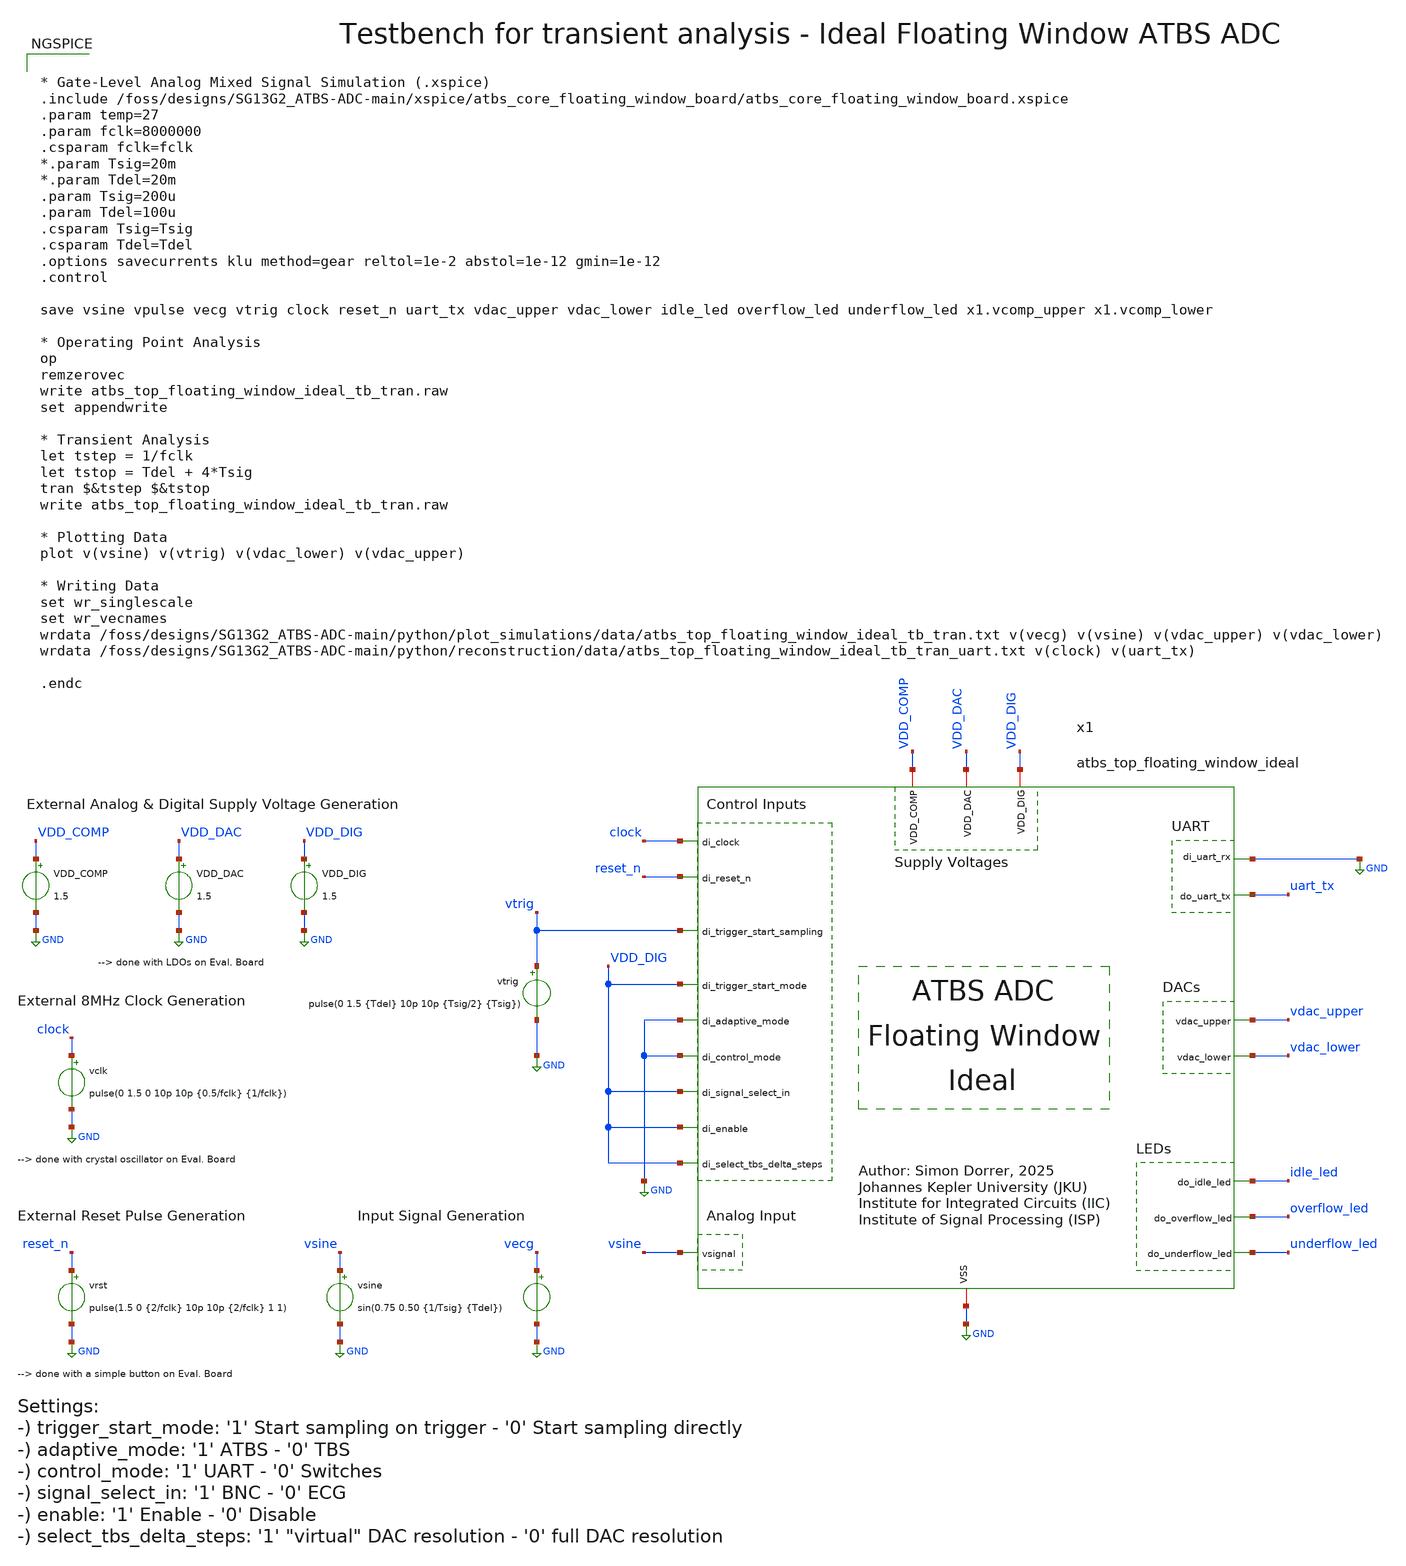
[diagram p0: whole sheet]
** sch_path: SG13G2_ATBS-ADC-main/xschem/top_level/testbenches/atbs_top_floating_window_ideal_tb_tran.sch
**.subckt atbs_top_floating_window_ideal_tb_tran
VDD_DAC VDD_DAC GND 1.5
VDD_COMP VDD_COMP GND 1.5
vsine vsine GND sin(0.75 0.50 {1/Tsig} {Tdel})
vclk clock GND pulse(0 1.5 0 10p 10p {0.5/fclk} {1/fclk})
vrst reset_n GND pulse(1.5 0 {2/fclk} 10p 10p {2/fclk} 1 1)
VDD_DIG VDD_DIG GND 1.5
x1 VDD_DIG VDD_COMP clock reset_n vtrig VDD_DAC VDD_DIG GND GND vsine VDD_DIG VDD_DIG VDD_DIG GND
+ uart_tx idle_led overflow_led underflow_led GND vdac_upper vdac_lower atbs_top_floating_window_ideal
vecg vecg GND dc 0 pwl(0.0 0.5958 3.910068426197458e-06 0.5985 7.820136852394917e-06 0.5982
+ 1.1730205278592374e-05 0.6038 1.5640273704789833e-05 0.61 1.9550342130987292e-05 0.6144 2.3460410557184748e-05 0.6189
+ 2.7370478983382207e-05 0.6204 3.1280547409579666e-05 0.6162 3.519061583577712e-05 0.6119 3.9100684261974585e-05 0.6106
+ 4.301075268817204e-05 0.6123 4.6920821114369496e-05 0.6199 5.083088954056696e-05 0.6267 5.4740957966764414e-05 0.6299
+ 5.865102639296188e-05 0.6252 6.256109481915933e-05 0.6185 6.647116324535679e-05 0.6128 7.038123167155424e-05 0.6143
+ 7.429130009775171e-05 0.6176 7.820136852394917e-05 0.6242 8.211143695014662e-05 0.6294 8.602150537634408e-05 0.6272
+ 8.993157380254154e-05 0.6273 9.384164222873899e-05 0.6275 9.775171065493646e-05 0.6317 0.00010166177908113392 0.6354
+ 0.00010557184750733137 0.6341 0.00010948191593352883 0.6258 0.00011339198435972628 0.6224 0.00011730205278592375 0.6222
+ 0.00012121212121212121 0.6297 0.00012512218963831867 0.6381 0.00012903225806451613 0.6441 0.00013294232649071358 0.649
+ 0.00013685239491691105 0.6455 0.0001407624633431085 0.6404 0.00014467253176930596 0.6344 0.00014858260019550343 0.6317
+ 0.00015249266862170087 0.6314 0.00015640273704789834 0.6377 0.00016031280547409578 0.6415 0.00016422287390029325 0.6412
+ 0.00016813294232649072 0.643 0.00017204301075268816 0.6462 0.00017595307917888563 0.6523 0.00017986314760508307 0.6546
+ 0.00018377321603128054 0.6538 0.00018768328445747798 0.6475 0.00019159335288367545 0.6412 0.00019550342130987292 0.6387
+ 0.00019941348973607036 0.6435 0.00020332355816226783 0.6518 0.00020723362658846528 0.6618 0.00021114369501466275 0.6648
+ 0.00021505376344086021 0.6571 0.00021896383186705766 0.6539 0.00022287390029325513 0.6536 0.00022678396871945257 0.6517
+ 0.00023069403714565004 0.6562 0.0002346041055718475 0.6624 0.00023851417399804495 0.6645 0.00024242424242424242 0.6631
+ 0.00024633431085043986 0.6616 0.00025024437927663733 0.6628 0.0002541544477028348 0.6643 0.00025806451612903227 0.6666
+ 0.0002619745845552297 0.6705 0.00026588465298142715 0.6671 0.0002697947214076246 0.6628 0.0002737047898338221 0.6546
+ 0.00027761485826001956 0.6579 0.000281524926686217 0.6719 0.00028543499511241445 0.6801 0.0002893450635386119 0.6801
+ 0.0002932551319648094 0.6725 0.00029716520039100685 0.6671 0.00030107526881720427 0.6592 0.00030498533724340174 0.6602
+ 0.0003088954056695992 0.6663 0.0003128054740957967 0.6668 0.00031671554252199415 0.6621 0.00032062561094819156 0.653
+ 0.00032453567937438903 0.6475 0.0003284457478005865 0.6456 0.00033235581622678397 0.6458 0.00033626588465298144 0.6442
+ 0.00034017595307917885 0.6438 0.0003440860215053763 0.6375 0.0003479960899315738 0.6288 0.00035190615835777126 0.6243
+ 0.00035581622678396873 0.6349 0.00035972629521016615 0.6464 0.0003636363636363636 0.6503 0.0003675464320625611 0.6447
+ 0.00037145650048875855 0.6388 0.00037536656891495597 0.6335 0.00037927663734115344 0.6324 0.0003831867057673509 0.6363
+ 0.0003870967741935484 0.6398 0.00039100684261974585 0.6507 0.00039491691104594326 0.661 0.00039882697947214073 0.6623
+ 0.0004027370478983382 0.6642 0.00040664711632453567 0.6686 0.00041055718475073314 0.6735 0.00041446725317693055 0.6756
+ 0.000418377321603128 0.6714 0.0004222873900293255 0.6609 0.00042619745845552296 0.6532 0.00043010752688172043 0.6527
+ 0.00043401759530791784 0.665 0.0004379276637341153 0.6815 0.0004418377321603128 0.6887 0.00044574780058651025 0.6869
+ 0.0004496578690127077 0.6736 0.00045356793743890514 0.6629 0.0004574780058651026 0.6561 0.0004613880742913001 0.6562
+ 0.00046529814271749754 0.6592 0.000469208211143695 0.6648 0.00047311827956989243 0.6671 0.0004770283479960899 0.6606
+ 0.00048093841642228737 0.6544 0.00048484848484848484 0.651 0.0004887585532746823 0.6519 0.0004926686217008797 0.6519
+ 0.0004965786901270772 0.6545 0.0005004887585532747 0.6524 0.0005043988269794721 0.6409 0.0005083088954056696 0.6268
+ 0.000512218963831867 0.6303 0.0005161290322580645 0.6493 0.000520039100684262 0.6638 0.0005239491691104594 0.6659
+ 0.0005278592375366569 0.6581 0.0005317693059628543 0.6451 0.0005356793743890518 0.6343 0.0005395894428152492 0.6278
+ 0.0005434995112414467 0.6257 0.0005474095796676442 0.6261 0.0005513196480938416 0.6239 0.0005552297165200391 0.6154
+ 0.0005591397849462365 0.6105 0.000563049853372434 0.6115 0.0005669599217986315 0.6197 0.0005708699902248289 0.6271
+ 0.0005747800586510264 0.6293 0.0005786901270772238 0.6242 0.0005826001955034212 0.6162 0.0005865102639296188 0.6101
+ 0.0005904203323558162 0.616 0.0005943304007820137 0.6276 0.0005982404692082111 0.6339 0.0006021505376344085 0.6337
+ 0.0006060606060606061 0.6271 0.0006099706744868035 0.6229 0.000613880742913001 0.6247 0.0006177908113391984 0.6293
+ 0.0006217008797653958 0.637 0.0006256109481915934 0.6436 0.0006295210166177908 0.643 0.0006334310850439883 0.6449
+ 0.0006373411534701857 0.6476 0.0006412512218963831 0.65 0.0006451612903225806 0.6564 0.0006490713587487781 0.6595
+ 0.0006529814271749756 0.6571 0.000656891495601173 0.6477 0.0006608015640273704 0.6374 0.0006647116324535679 0.629
+ 0.0006686217008797654 0.6292 0.0006725317693059629 0.6357 0.0006764418377321603 0.6455 0.0006803519061583577 0.6493
+ 0.0006842619745845552 0.6455 0.0006881720430107526 0.6424 0.0006920821114369502 0.6339 0.0006959921798631476 0.625
+ 0.000699902248289345 0.6209 0.0007038123167155425 0.6215 0.0007077223851417399 0.6246 0.0007116324535679375 0.6282
+ 0.0007155425219941349 0.6317 0.0007194525904203323 0.6381 0.0007233626588465298 0.6501 0.0007272727272727272 0.6566
+ 0.0007311827956989248 0.6539 0.0007350928641251222 0.6482 0.0007390029325513196 0.6382 0.0007429130009775171 0.6283
+ 0.0007468230694037145 0.6334 0.0007507331378299119 0.6477 0.0007546432062561095 0.6578 0.0007585532746823069 0.6583
+ 0.0007624633431085044 0.6561 0.0007663734115347018 0.6535 0.0007702834799608992 0.6449 0.0007741935483870968 0.639
+ 0.0007781036168132942 0.6398 0.0007820136852394917 0.6485 0.0007859237536656891 0.6535 0.0007898338220918865 0.6513
+ 0.000793743890518084 0.6483 0.0007976539589442815 0.6442 0.000801564027370479 0.6384 0.0008054740957966764 0.6345
+ 0.0008093841642228738 0.6283 0.0008132942326490713 0.6215 0.0008172043010752688 0.6179 0.0008211143695014663 0.6204
+ 0.0008250244379276637 0.6304 0.0008289345063538611 0.6402 0.0008328445747800586 0.6415 0.000836754643206256 0.6331
+ 0.0008406647116324536 0.6263 0.000844574780058651 0.6245 0.0008484848484848484 0.6254 0.0008523949169110459 0.6298
+ 0.0008563049853372433 0.632 0.0008602150537634409 0.635 0.0008641251221896383 0.6377 0.0008680351906158357 0.6337
+ 0.0008719452590420332 0.6286 0.0008758553274682306 0.6293 0.0008797653958944282 0.6387 0.0008836754643206256 0.6455
+ 0.000887585532746823 0.6419 0.0008914956011730205 0.631 0.0008954056695992179 0.6165 0.0008993157380254154 0.6051
+ 0.0009032258064516129 0.6102 0.0009071358748778103 0.6259 0.0009110459433040078 0.6371 0.0009149560117302052 0.6451
+ 0.0009188660801564027 0.6449 0.0009227761485826002 0.642 0.0009266862170087976 0.6356 0.0009305962854349951 0.629
+ 0.0009345063538611925 0.6259 0.00093841642228739 0.6271 0.0009423264907135874 0.6295 0.0009462365591397849 0.6266
+ 0.0009501466275659824 0.6267 0.0009540566959921798 0.6312 0.0009579667644183773 0.639 0.0009618768328445747 0.6441
+ 0.0009657869012707722 0.6462 0.0009696969696969697 0.6429 0.0009736070381231671 0.6387 0.0009775171065493646 0.6335
+ 0.000981427174975562 0.6408 0.0009853372434017594 0.6532 0.0009892473118279569 0.6535 0.0009931573802541545 0.6446
+ 0.000997067448680352 0.6334 0.0010009775171065493 0.6282 0.0010048875855327467 0.6231 0.0010087976539589442 0.6265
+ 0.0010127077223851418 0.6331 0.0010166177908113392 0.6414 0.0010205278592375366 0.6474 0.001024437927663734 0.645
+ 0.0010283479960899314 0.639 0.001032258064516129 0.632 0.0010361681329423265 0.6239 0.001040078201368524 0.6222
+ 0.0010439882697947213 0.627 0.0010478983382209187 0.6249 0.0010518084066471164 0.6219 0.0010557184750733138 0.617
+ 0.0010596285434995112 0.6225 0.0010635386119257086 0.6306 0.001067448680351906 0.6294 0.0010713587487781037 0.6244
+ 0.001075268817204301 0.6201 0.0010791788856304985 0.6194 0.001083088954056696 0.6232 0.0010869990224828933 0.6285
+ 0.001090909090909091 0.6282 0.0010948191593352884 0.6291 0.0010987292277614858 0.6302 0.0011026392961876832 0.6277
+ 0.0011065493646138806 0.6253 0.0011104594330400782 0.6244 0.0011143695014662757 0.6257 0.001118279569892473 0.6244
+ 0.0011221896383186705 0.6272 0.001126099706744868 0.6286 0.0011300097751710655 0.6217 0.001133919843597263 0.6145
+ 0.0011378299120234604 0.6168 0.0011417399804496578 0.6251 0.0011456500488758552 0.6334 0.0011495601173020528 0.6396
+ 0.0011534701857282502 0.6362 0.0011573802541544477 0.6278 0.001161290322580645 0.616 0.0011652003910068425 0.6127
+ 0.0011691104594330401 0.6151 0.0011730205278592375 0.6206 0.001176930596285435 0.6274 0.0011808406647116324 0.6268
+ 0.0011847507331378298 0.6251 0.0011886608015640274 0.6268 0.0011925708699902248 0.6305 0.0011964809384164222 0.6318
+ 0.0012003910068426197 0.6323 0.001204301075268817 0.6264 0.0012082111436950147 0.6211 0.0012121212121212121 0.6198
+ 0.0012160312805474095 0.6259 0.001219941348973607 0.632 0.0012238514173998044 0.633 0.001227761485826002 0.636
+ 0.0012316715542521994 0.6335 0.0012355816226783968 0.6281 0.0012394916911045942 0.6258 0.0012434017595307917 0.6319
+ 0.0012473118279569893 0.637 0.0012512218963831867 0.6389 0.0012551319648093841 0.6384 0.0012590420332355815 0.6327
+ 0.001262952101661779 0.6333 0.0012668621700879766 0.6398 0.001270772238514174 0.6508 0.0012746823069403714 0.6614
+ 0.0012785923753665688 0.6629 0.0012825024437927662 0.6554 0.0012864125122189639 0.6487 0.0012903225806451613 0.6476
+ 0.0012942326490713587 0.6564 0.0012981427174975561 0.6702 0.0013020527859237535 0.679 0.0013059628543499512 0.6801
+ 0.0013098729227761486 0.6732 0.001313782991202346 0.6701 0.0013176930596285434 0.6706 0.0013216031280547408 0.6722
+ 0.0013255131964809385 0.6724 0.0013294232649071359 0.6741 0.0013333333333333333 0.6714 0.0013372434017595307 0.6649
+ 0.0013411534701857281 0.6606 0.0013450635386119258 0.6595 0.0013489736070381232 0.6638 0.0013528836754643206 0.6658
+ 0.001356793743890518 0.664 0.0013607038123167154 0.6556 0.001364613880742913 0.6455 0.0013685239491691105 0.6396
+ 0.0013724340175953079 0.6482 0.0013763440860215053 0.6591 0.0013802541544477027 0.662 0.0013841642228739003 0.6594
+ 0.0013880742913000978 0.6508 0.0013919843597262952 0.6443 0.0013958944281524926 0.6412 0.00139980449657869 0.6391
+ 0.0014037145650048876 0.64 0.001407624633431085 0.6457 0.0014115347018572825 0.6474 0.0014154447702834799 0.6436
+ 0.0014193548387096773 0.6374 0.001423264907135875 0.6343 0.0014271749755620723 0.6352 0.0014310850439882698 0.6353
+ 0.0014349951124144672 0.6288 0.0014389051808406646 0.6168 0.0014428152492668622 0.5964 0.0014467253176930596 0.5828
+ 0.001450635386119257 0.5848 0.0014545454545454545 0.5932 0.0014584555229716519 0.5988 0.0014623655913978495 0.6013
+ 0.001466275659824047 0.5993 0.0014701857282502443 0.5925 0.0014740957966764417 0.5869 0.0014780058651026392 0.5871
+ 0.0014819159335288368 0.5902 0.0014858260019550342 0.5972 0.0014897360703812316 0.6052 0.001493646138807429 0.6056
+ 0.0014975562072336265 0.6105 0.0015014662756598239 0.6175 0.0015053763440860215 0.6238 0.001509286412512219 0.6242
+ 0.0015131964809384163 0.6232 0.0015171065493646137 0.6199 0.0015210166177908112 0.6155 0.0015249266862170088 0.6119
+ 0.0015288367546432062 0.6176 0.0015327468230694036 0.6299 0.001536656891495601 0.6393 0.0015405669599217985 0.6419
+ 0.001544477028347996 0.6374 0.0015483870967741935 0.6291 0.001552297165200391 0.6229 0.0015562072336265883 0.6219
+ 0.0015601173020527857 0.625 0.0015640273704789834 0.6286 0.0015679374389051808 0.6267 0.0015718475073313782 0.6183
+ 0.0015757575757575756 0.6137 0.001579667644183773 0.6122 0.0015835777126099707 0.6148 0.001587487781036168 0.6175
+ 0.0015913978494623655 0.6181 0.001595307917888563 0.6126 0.0015992179863147603 0.6028 0.001603128054740958 0.596
+ 0.0016070381231671554 0.6044 0.0016109481915933528 0.6182 0.0016148582600195502 0.6263 0.0016187683284457476 0.6232
+ 0.0016226783968719453 0.6123 0.0016265884652981427 0.6041 0.00163049853372434 0.5979 0.0016344086021505375 0.5952
+ 0.001638318670576735 0.5965 0.0016422287390029325 0.6022 0.00164613880742913 0.6069 0.0016500488758553274 0.6035
+ 0.0016539589442815248 0.603 0.0016578690127077222 0.6032 0.0016617790811339198 0.6091 0.0016656891495601173 0.6148
+ 0.0016695992179863147 0.6158 0.001673509286412512 0.6102 0.0016774193548387095 0.599 0.0016813294232649071 0.5905
+ 0.0016852394916911045 0.5946 0.001689149560117302 0.6083 0.0016930596285434994 0.6121 0.0016969696969696968 0.6133
+ 0.0017008797653958944 0.6071 0.0017047898338220918 0.5998 0.0017086999022482893 0.5943 0.0017126099706744867 0.5917
+ 0.001716520039100684 0.5903 0.0017204301075268817 0.5931 0.0017243401759530791 0.5958 0.0017282502443792765 0.5931
+ 0.001732160312805474 0.5892 0.0017360703812316714 0.5865 0.001739980449657869 0.5906 0.0017438905180840664 0.593
+ 0.0017478005865102638 0.5958 0.0017517106549364613 0.5971 0.0017556207233626587 0.592 0.0017595307917888563 0.5844
+ 0.0017634408602150537 0.5882 0.0017673509286412511 0.5988 0.0017712609970674485 0.6044 0.001775171065493646 0.6045
+ 0.0017790811339198436 0.6 0.001782991202346041 0.5917 0.0017869012707722384 0.5876 0.0017908113391984358 0.5904
+ 0.0017947214076246333 0.5996 0.0017986314760508309 0.6059 0.0018025415444770283 0.6095 0.0018064516129032257 0.6109
+ 0.0018103616813294231 0.6095 0.0018142717497556205 0.6109 0.0018181818181818182 0.6174 0.0018220918866080156 0.6238
+ 0.001826001955034213 0.6278 0.0018299120234604104 0.6264 0.0018338220918866078 0.6177 0.0018377321603128055 0.6093
+ 0.0018416422287390029 0.6156 0.0018455522971652003 0.6254 0.0018494623655913977 0.6305 0.0018533724340175951 0.6326
+ 0.0018572825024437928 0.6278 0.0018611925708699902 0.6259 0.0018651026392961876 0.6247 0.001869012707722385 0.6251
+ 0.0018729227761485824 0.629 0.00187683284457478 0.6279 0.0018807429130009775 0.6217 0.0018846529814271749 0.6134
+ 0.0018885630498533723 0.6091 0.0018924731182795697 0.6093 0.0018963831867057673 0.6123 0.0019002932551319648 0.6172
+ 0.0019042033235581622 0.6183 0.0019081133919843596 0.6119 0.001912023460410557 0.6026 0.0019159335288367546 0.5924
+ 0.001919843597262952 0.5961 0.0019237536656891495 0.6095 0.0019276637341153469 0.6152 0.0019315738025415443 0.6082
+ 0.001935483870967742 0.5974 0.0019393939393939393 0.5894 0.0019433040078201368 0.5836 0.0019472140762463342 0.5864
+ 0.0019511241446725316 0.5916 0.0019550342130987292 0.5981 0.0019589442815249264 0.5983 0.001962854349951124 0.592
+ 0.0019667644183773217 0.58 0.001970674486803519 0.5702 0.0019745845552297165 0.5708 0.0019784946236559137 0.5752
+ 0.0019824046920821113 0.5777 0.001986314760508309 0.578 0.001990224828934506 0.5793 0.001994134897360704 0.5826
+ 0.001998044965786901 0.5978 0.0020019550342130986 0.6213 0.0020058651026392963 0.6388 0.0020097751710654935 0.6554
+ 0.002013685239491691 0.6703 0.0020175953079178883 0.6918 0.002021505376344086 0.7181 0.0020254154447702836 0.7519
+ 0.0020293255131964808 0.7929 0.0020332355816226784 0.8382 0.0020371456500488756 0.8855 0.0020410557184750732 0.9325
+ 0.002044965786901271 0.9836 0.002048875855327468 1.0344 0.0020527859237536657 1.0885 0.002056695992179863 1.1466
+ 0.0020606060606060605 1.2035 0.002064516129032258 1.2532 0.0020684261974584553 1.3 0.002072336265884653 1.2942
+ 0.00207624633431085 1.2885 0.002080156402737048 1.2826 0.0020840664711632454 1.2769 0.0020879765395894426 1.2714
+ 0.0020918866080156403 1.2668 0.0020957966764418375 1.2598 0.002099706744868035 1.2536 0.0021036168132942327 1.2482
+ 0.00210752688172043 1.2423 0.0021114369501466276 1.2365 0.0021153470185728248 1.231 0.0021192570869990224 1.2252
+ 0.00212316715542522 1.2196 0.0021270772238514172 1.2133 0.002130987292277615 1.1967 0.002134897360703812 1.1296
+ 0.0021388074291300097 1.0419 0.0021427174975562073 0.9281 0.0021466275659824045 0.8036 0.002150537634408602 0.6811
+ 0.0021544477028347993 0.5654 0.002158357771260997 0.4556 0.0021622678396871946 0.3608 0.002166177908113392 0.2826
+ 0.0021700879765395894 0.217 0.0021739980449657866 0.1684 0.0021779081133919843 0.1376 0.002181818181818182 0.1154
+ 0.002185728250244379 0.1 0.0021896383186705767 0.1009 0.002193548387096774 0.1122 0.0021974584555229716 0.1309
+ 0.002201368523949169 0.159 0.0022052785923753664 0.1921 0.002209188660801564 0.2272 0.0022130987292277612 0.2652
+ 0.002217008797653959 0.2953 0.0022209188660801565 0.3131 0.0022248289345063537 0.3249 0.0022287390029325513 0.3361
+ 0.0022326490713587485 0.3577 0.002236559139784946 0.382 0.0022404692082111438 0.3989 0.002244379276637341 0.4072
+ 0.0022482893450635386 0.4052 0.002252199413489736 0.4011 0.0022561094819159334 0.3957 0.002260019550342131 0.3998
+ 0.0022639296187683283 0.4047 0.002267839687194526 0.4115 0.002271749755620723 0.4171 0.0022756598240469207 0.4189
+ 0.0022795698924731184 0.4211 0.0022834799608993156 0.4295 0.002287390029325513 0.4436 0.0022913000977517104 0.453
+ 0.002295210166177908 0.4584 0.0022991202346041057 0.4591 0.002303030303030303 0.4579 0.0023069403714565005 0.4602
+ 0.0023108504398826977 0.4714 0.0023147605083088953 0.4834 0.002318670576735093 0.487 0.00232258064516129 0.4845
+ 0.0023264907135874878 0.4786 0.002330400782013685 0.4672 0.0023343108504398826 0.4578 0.0023382209188660802 0.4515
+ 0.0023421309872922774 0.4524 0.002346041055718475 0.4611 0.0023499511241446723 0.4644 0.00235386119257087 0.4609
+ 0.0023577712609970675 0.4619 0.0023616813294232647 0.4655 0.0023655913978494624 0.4743 0.0023695014662756596 0.4811
+ 0.002373411534701857 0.4826 0.002377321603128055 0.4771 0.002381231671554252 0.4694 0.0023851417399804497 0.4687
+ 0.002389051808406647 0.478 0.0023929618768328445 0.4897 0.002396871945259042 0.4957 0.0024007820136852393 0.5
+ 0.002404692082111437 0.4979 0.002408602150537634 0.4968 0.0024125122189638318 0.4965 0.0024164222873900294 0.5002
+ 0.0024203323558162266 0.5095 0.0024242424242424242 0.5165 0.0024281524926686214 0.5223 0.002432062561094819 0.5205
+ 0.0024359726295210167 0.5186 0.002439882697947214 0.5205 0.0024437927663734115 0.5281 0.0024477028347996087 0.5415
+ 0.0024516129032258064 0.5447 0.002455522971652004 0.5397 0.002459433040078201 0.5315 0.002463343108504399 0.5274
+ 0.002467253176930596 0.535 0.0024711632453567937 0.5484 0.0024750733137829913 0.5567 0.0024789833822091885 0.5636
+ 0.002482893450635386 0.5627 0.0024868035190615833 0.5603 0.002490713587487781 0.5545 0.0024946236559139786 0.5528
+ 0.0024985337243401758 0.5518 0.0025024437927663734 0.553 0.0025063538611925706 0.5516 0.0025102639296187682 0.5499
+ 0.002514173998044966 0.5449 0.002518084066471163 0.5471 0.0025219941348973607 0.5603 0.002525904203323558 0.5685
+ 0.0025298142717497555 0.572 0.002533724340175953 0.5676 0.0025376344086021504 0.5602 0.002541544477028348 0.5534
+ 0.002545454545454545 0.5604 0.002549364613880743 0.5731 0.0025532746823069405 0.5841 0.0025571847507331377 0.5875
+ 0.0025610948191593353 0.5869 0.0025650048875855325 0.5827 0.00256891495601173 0.5792 0.0025728250244379277 0.5812
+ 0.002576735092864125 0.5859 0.0025806451612903226 0.5908 0.0025845552297165198 0.5914 0.0025884652981427174 0.5866
+ 0.002592375366568915 0.5871 0.0025962854349951122 0.593 0.00260019550342131 0.5996 0.002604105571847507 0.6003
+ 0.0026080156402737047 0.5944 0.0026119257086999023 0.5892 0.0026158357771260995 0.5891 0.002619745845552297 0.5901
+ 0.0026236559139784944 0.5936 0.002627565982404692 0.6017 0.0026314760508308896 0.6066 0.002635386119257087 0.6024
+ 0.0026392961876832845 0.5985 0.0026432062561094817 0.5996 0.0026471163245356793 0.5982 0.002651026392961877 0.5962
+ 0.002654936461388074 0.5969 0.0026588465298142717 0.6024 0.002662756598240469 0.6041 0.0026666666666666666 0.6056
+ 0.002670576735092864 0.6091 0.0026744868035190614 0.6126 0.002678396871945259 0.6169 0.0026823069403714562 0.6229
+ 0.002686217008797654 0.6264 0.0026901270772238515 0.6181 0.0026940371456500487 0.6077 0.0026979472140762463 0.6017
+ 0.0027018572825024435 0.6124 0.002705767350928641 0.6275 0.002709677419354839 0.6336 0.002713587487781036 0.6293
+ 0.0027174975562072336 0.619 0.002721407624633431 0.6046 0.0027253176930596285 0.5948 0.002729227761485826 0.5948
+ 0.0027331378299120233 0.5995 0.002737047898338221 0.5994 0.002740957966764418 0.595 0.0027448680351906157 0.5861
+ 0.0027487781036168134 0.5802 0.0027526881720430106 0.5825 0.002756598240469208 0.5913 0.0027605083088954054 0.6001
+ 0.002764418377321603 0.6049 0.0027683284457478007 0.6012 0.002772238514173998 0.5907 0.0027761485826001955 0.585
+ 0.0027800586510263927 0.5939 0.0027839687194525903 0.607 0.002787878787878788 0.6169 0.002791788856304985 0.625
+ 0.002795698924731183 0.6239 0.00279960899315738 0.6239 0.0028035190615835776 0.621 0.0028074291300097753 0.624
+ 0.0028113391984359725 0.6299 0.00281524926686217 0.6359 0.0028191593352883673 0.6377 0.002823069403714565 0.6335
+ 0.0028269794721407625 0.6341 0.0028308895405669597 0.6396 0.0028347996089931574 0.6458 0.0028387096774193546 0.6499
+ 0.002842619745845552 0.6522 0.00284652981427175 0.6458 0.002850439882697947 0.6395 0.0028543499511241447 0.6349
+ 0.002858260019550342 0.6389 0.0028621700879765395 0.6482 0.002866080156402737 0.6495 0.0028699902248289343 0.6445
+ 0.002873900293255132 0.6378 0.002877810361681329 0.6328 0.002881720430107527 0.6295 0.0028856304985337244 0.6306
+ 0.0028895405669599216 0.6367 0.0028934506353861193 0.6514 0.0028973607038123165 0.6632 0.002901270772238514 0.6617
+ 0.0029051808406647117 0.6624 0.002909090909090909 0.6643 0.0029130009775171065 0.6646 0.0029169110459433037 0.6642
+ 0.0029208211143695014 0.6612 0.002924731182795699 0.6518 0.002928641251221896 0.6433 0.002932551319648094 0.6426
+ 0.002936461388074291 0.6522 0.0029403714565004887 0.6656 0.0029442815249266863 0.6728 0.0029481915933528835 0.6738
+ 0.002952101661779081 0.6692 0.0029560117302052783 0.666 0.002959921798631476 0.667 0.0029638318670576736 0.6666
+ 0.002967741935483871 0.6644 0.0029716520039100684 0.6657 0.0029755620723362656 0.6638 0.0029794721407624633 0.6568
+ 0.002983382209188661 0.6551 0.002987292277614858 0.6566 0.0029912023460410557 0.6631 0.002995112414467253 0.6689
+ 0.0029990224828934505 0.6677 0.0030029325513196477 0.662 0.0030068426197458454 0.6549 0.003010752688172043 0.6551
+ 0.00301466275659824 0.6691 0.003018572825024438 0.6819 0.003022482893450635 0.6912 0.0030263929618768327 0.695
+ 0.0030303030303030303 0.6932 0.0030342130987292275 0.6952 0.003038123167155425 0.7034 0.0030420332355816223 0.7138
+ 0.00304594330400782 0.7209 0.0030498533724340176 0.7327 0.003053763440860215 0.7376 0.0030576735092864124 0.7351
+ 0.0030615835777126096 0.7336 0.0030654936461388073 0.7328 0.003069403714565005 0.7369 0.003073313782991202 0.7404
+ 0.0030772238514173997 0.7446 0.003081133919843597 0.7451 0.0030850439882697945 0.7433 0.003088954056695992 0.743
+ 0.0030928641251221894 0.7505 0.003096774193548387 0.7563 0.003100684261974584 0.7588 0.003104594330400782 0.7581
+ 0.0031085043988269795 0.7551 0.0031124144672531767 0.7517 0.0031163245356793743 0.7522 0.0031202346041055715 0.7564
+ 0.003124144672531769 0.7643 0.0031280547409579668 0.7735 0.003131964809384164 0.7788 0.0031358748778103616 0.7806
+ 0.003139784946236559 0.7857 0.0031436950146627564 0.7898 0.003147605083088954 0.7975 0.0031515151515151513 0.8073
+ 0.003155425219941349 0.8131 0.003159335288367546 0.816 0.0031632453567937437 0.8181 0.0031671554252199413 0.8195
+ 0.0031710654936461385 0.8293 0.003174975562072336 0.8431 0.0031788856304985334 0.8512 0.003182795698924731 0.8559
+ 0.0031867057673509286 0.8577 0.003190615835777126 0.8607 0.0031945259042033235 0.8584 0.0031984359726295207 0.8553
+ 0.0032023460410557183 0.8529 0.003206256109481916 0.849 0.003210166177908113 0.8428 0.0032140762463343108 0.8393
+ 0.003217986314760508 0.8444 0.0032218963831867056 0.8496 0.0032258064516129032 0.8541 0.0032297165200391004 0.8575
+ 0.003233626588465298 0.8566 0.0032375366568914953 0.8492 0.003241446725317693 0.8411 0.0032453567937438905 0.8339
+ 0.0032492668621700877 0.8355 0.0032531769305962853 0.8438 0.0032570869990224825 0.849 0.00326099706744868 0.8448
+ 0.003264907135874878 0.8321 0.003268817204301075 0.8248 0.0032727272727272726 0.8203 0.00327663734115347 0.8166
+ 0.0032805474095796675 0.8224 0.003284457478005865 0.8301 0.0032883675464320623 0.8385 0.00329227761485826 0.8371
+ 0.003296187683284457 0.8262 0.0033000977517106548 0.8151 0.0033040078201368524 0.8133 0.0033079178885630496 0.8143
+ 0.0033118279569892472 0.8109 0.0033157380254154444 0.8008 0.003319648093841642 0.7874 0.0033235581622678397 0.7754
+ 0.003327468230694037 0.7759 0.0033313782991202345 0.7809 0.0033352883675464317 0.7835 0.0033391984359726293 0.7746
+ 0.003343108504398827 0.7588 0.003347018572825024 0.75 0.003350928641251222 0.7429 0.003354838709677419 0.7373
+ 0.0033587487781036166 0.7301 0.0033626588465298143 0.727 0.0033665689149560115 0.7161 0.003370478983382209 0.696
+ 0.0033743890518084063 0.6794 0.003378299120234604 0.6727 0.0033822091886608016 0.6671 0.0033861192570869988 0.6623
+ 0.0033900293255131964 0.6511 0.0033939393939393936 0.6306 0.0033978494623655912 0.6095 0.003401759530791789 0.5925
+ 0.003405669599217986 0.5872 0.0034095796676441837 0.5844 0.003413489736070381 0.5781 0.0034173998044965785 0.5696
+ 0.003421309872922776 0.5558 0.0034252199413489733 0.541 0.003429130009775171 0.5191 0.003433040078201368 0.5036
+ 0.003436950146627566 0.4921 0.0034408602150537634 0.4852 0.0034447702834799606 0.4715 0.0034486803519061583 0.4564
+ 0.0034525904203323555 0.4464 0.003456500488758553 0.4411 0.0034604105571847507 0.4438 0.003464320625610948 0.4418
+ 0.0034682306940371456 0.4314 0.0034721407624633428 0.4168 0.0034760508308895404 0.4047 0.003479960899315738 0.3946
+ 0.0034838709677419352 0.3934 0.003487781036168133 0.3956 0.00349169110459433 0.3906 0.0034956011730205277 0.3816
+ 0.0034995112414467253 0.3725 0.0035034213098729225 0.3634 0.00350733137829912 0.3497 0.0035112414467253173 0.3389
+ 0.003515151515151515 0.3377 0.0035190615835777126 0.3388 0.00352297165200391 0.3349 0.0035268817204301074 0.328
+ 0.0035307917888563046 0.3205 0.0035347018572825023 0.3179 0.0035386119257087 0.3206 0.003542521994134897 0.3233
+ 0.0035464320625610947 0.3216 0.003550342130987292 0.3157 0.0035542521994134896 0.3059 0.003558162267839687 0.2951
+ 0.0035620723362658844 0.2939 0.003565982404692082 0.3011 0.0035698924731182792 0.3006 0.003573802541544477 0.2988
+ 0.0035777126099706745 0.2972 0.0035816226783968717 0.295 0.0035855327468230693 0.2941 0.0035894428152492665 0.2993
+ 0.003593352883675464 0.3056 0.0035972629521016618 0.3162 0.003601173020527859 0.3249 0.0036050830889540566 0.3257
+ 0.003608993157380254 0.3269 0.0036129032258064514 0.3268 0.003616813294232649 0.3276 0.0036207233626588463 0.331
+ 0.003624633431085044 0.3277 0.003628543499511241 0.3258 0.0036324535679374387 0.3218 0.0036363636363636364 0.3131
+ 0.0036402737047898336 0.3214 0.003644183773216031 0.3389 0.0036480938416422284 0.3469 0.003652003910068426 0.3501
+ 0.0036559139784946237 0.3423 0.003659824046920821 0.3349 0.0036637341153470185 0.3292 0.0036676441837732157 0.3288
+ 0.0036715542521994133 0.3339 0.003675464320625611 0.3474 0.003679374389051808 0.3572 0.0036832844574780058 0.3568
+ 0.003687194525904203 0.3557 0.0036911045943304006 0.3541 0.0036950146627565982 0.3578 0.0036989247311827954 0.3649
+ 0.003702834799608993 0.3709 0.0037067448680351903 0.3746 0.003710654936461388 0.3741 0.0037145650048875855 0.3726
+ 0.0037184750733137827 0.3857 0.0037223851417399804 0.4015 0.0037262952101661776 0.4087 0.003730205278592375 0.4071
+ 0.003734115347018573 0.4036 0.00373802541544477 0.4005 0.0037419354838709677 0.4027 0.003745845552297165 0.4112
+ 0.0037497556207233625 0.4201 0.00375366568914956 0.4278 0.0037575757575757573 0.4325 0.003761485826001955 0.433
+ 0.003765395894428152 0.4363 0.0037693059628543498 0.4351 0.0037732160312805474 0.4349 0.0037771260997067446 0.4367
+ 0.0037810361681329422 0.4386 0.0037849462365591394 0.4376 0.003788856304985337 0.4372 0.0037927663734115347 0.4351
+ 0.003796676441837732 0.4419 0.0038005865102639295 0.4512 0.0038044965786901267 0.4559 0.0038084066471163244 0.457
+ 0.003812316715542522 0.4584 0.003816226783968719 0.4638 0.003820136852394917 0.469 0.003824046920821114 0.4758
+ 0.0038279569892473117 0.4785 0.0038318670576735093 0.4824 0.0038357771260997065 0.4866 0.003839687194525904 0.4862
+ 0.0038435972629521013 0.4888 0.003847507331378299 0.4946 0.0038514173998044966 0.5018 0.0038553274682306938 0.511
+ 0.0038592375366568914 0.5156 0.0038631476050830886 0.516 0.0038670576735092862 0.5103 0.003870967741935484 0.5061
+ 0.003874877810361681 0.5146 0.0038787878787878787 0.5265 0.003882697947214076 0.5318 0.0038866080156402735 0.5323
+ 0.003890518084066471 0.5304 0.0038944281524926684 0.5326 0.003898338220918866 0.5327 0.003902248289345063 0.5336
+ 0.003906158357771261 0.5339 0.0039100684261974585 0.5347 0.003913978494623656 0.5356 0.003917888563049853 0.5347
+ 0.003921798631476051 0.5355 0.003925708699902248 0.5417 0.003929618768328445 0.5518 0.003933528836754643 0.5575
+ 0.003937438905180841 0.5562 0.003941348973607038 0.5498 0.003945259042033236 0.5394 0.003949169110459433 0.5324
+ 0.00395307917888563 0.5382 0.003956989247311827 0.5497 0.0039608993157380255 0.5578 0.003964809384164223 0.5558
+ 0.00396871945259042 0.554 0.003972629521016618 0.5549 0.003976539589442815 0.5578 0.003980449657869012 0.5618
+ 0.00398435972629521 0.5665 0.003988269794721408 0.5743 0.003992179863147605 0.5782 0.003996089931573802 0.5752 0.004
+ 0.5699 )
vtrig vtrig GND pulse(0 1.5 {Tdel} 10p 10p {Tsig/2} {Tsig})
**** begin user architecture code


* Gate-Level Analog Mixed Signal Simulation (.xspice)
.include /foss/designs/SG13G2_ATBS-ADC-main/xspice/atbs_core_floating_window_board/atbs_core_floating_window_board.xspice
.param temp=27
.param fclk=8000000
.csparam fclk=fclk
*.param Tsig=20m
*.param Tdel=20m
.param Tsig=200u
.param Tdel=100u
.csparam Tsig=Tsig
.csparam Tdel=Tdel
.options savecurrents klu method=gear reltol=1e-2 abstol=1e-12 gmin=1e-12
.control

save vsine vpulse vecg vtrig clock reset_n uart_tx vdac_upper vdac_lower idle_led overflow_led
+ underflow_led x1.vcomp_upper x1.vcomp_lower

* Operating Point Analysis
op
remzerovec
write atbs_top_floating_window_ideal_tb_tran.raw
set appendwrite

* Transient Analysis
let tstep = 1/fclk
let tstop = Tdel + 4*Tsig
tran $&tstep $&tstop
write atbs_top_floating_window_ideal_tb_tran.raw

* Plotting Data
plot v(vsine) v(vtrig) v(vdac_lower) v(vdac_upper)

* Writing Data
set wr_singlescale
set wr_vecnames
wrdata
+ /foss/designs/SG13G2_ATBS-ADC-main/python/plot_simulations/data/atbs_top_floating_window_ideal_tb_tran.txt v(vecg) v(vsine) v(vdac_upper) v(vdac_lower)
wrdata
+ /foss/designs/SG13G2_ATBS-ADC-main/python/reconstruction/data/atbs_top_floating_window_ideal_tb_tran_uart.txt v(clock) v(uart_tx)

.endc


.lib cornerMOSlv.lib mos_tt
.lib cornerRES.lib res_typ

**** end user architecture code
**.ends

* expanding   symbol:  top_level/atbs_top_floating_window_ideal.sym # of pins=21
** sym_path: SG13G2_ATBS-ADC-main/xschem/top_level/atbs_top_floating_window_ideal.sym
** sch_path: SG13G2_ATBS-ADC-main/xschem/top_level/atbs_top_floating_window_ideal.sch
.subckt atbs_top_floating_window_ideal VDD_DIG VDD_COMP di_clock di_reset_n
+ di_trigger_start_sampling VDD_DAC di_trigger_start_mode di_adaptive_mode di_control_mode vsignal di_signal_select_in
+ di_enable di_select_tbs_delta_steps di_uart_rx do_uart_tx do_idle_led do_overflow_led do_underflow_led VSS
+ vdac_upper vdac_lower
*.iopin VDD_DIG
*.iopin VSS
*.iopin VDD_COMP
*.ipin vsignal
*.ipin di_clock
*.ipin di_reset_n
*.iopin VDD_DAC
*.ipin di_uart_rx
*.opin do_uart_tx
*.ipin di_trigger_start_sampling
*.ipin di_trigger_start_mode
*.ipin di_adaptive_mode
*.ipin di_control_mode
*.ipin di_signal_select_in
*.ipin di_enable
*.ipin di_select_tbs_delta_steps
*.opin do_idle_led
*.opin do_overflow_led
*.opin do_underflow_led
*.opin vdac_upper
*.opin vdac_lower
x5 VDD_DIG VSS di_adaptive_mode di_clock vcomp_lower vcomp_upper di_control_mode net9 net10 net11
+ net12 net13 net14 net15 net16 net1 net2 net3 net4 net5 net6 net7 net8 di_enable do_idle_led
+ do_overflow_led di_reset_n di_select_tbs_delta_steps di_signal_select_in di_trigger_start_mode
+ di_trigger_start_sampling di_uart_rx do_uart_tx do_underflow_led atbs_core_floating_window_board
x3 VDD_DAC net2 net5 net1 net3 net4 net8 net6 net7 vdac_upper VSS dac_ideal tsettle=10n
x4 VDD_DAC net10 net13 net9 net11 net12 net16 net14 net15 vdac_lower VSS dac_ideal tsettle=10n
x1 vsignal vdac_upper VDD_COMP vcomp_upper VSS CT_comparator_ideal A=10k Rin=10Meg Rout=100 Pdc=
+ Vcm=0.75 Voffs=1m tpd=1n
x2 vsignal vdac_lower VDD_COMP vcomp_lower VSS CT_comparator_ideal A=10k Rin=10Meg Rout=100 Pdc=
+ Vcm=0.75 Voffs=1m tpd=1n
.ends


* expanding   symbol:  dac/ideal/dac_ideal.sym # of pins=11
** sym_path: SG13G2_ATBS-ADC-main/xschem/dac/ideal/dac_ideal.sym
** sch_path: SG13G2_ATBS-ADC-main/xschem/dac/ideal/dac_ideal.sch
.subckt dac_ideal VDD di_D1 di_D4 di_D0 di_D2 di_D3 di_D7 di_D5 di_D6 vdac_out VSS  tsettle=10n
*.opin vdac_out
*.ipin di_D0
*.iopin VSS
*.iopin VDD
*.ipin di_D1
*.ipin di_D2
*.ipin di_D3
*.ipin di_D4
*.ipin di_D5
*.ipin di_D6
*.ipin di_D7
R1 net1 VSS 3925 m=1
G1 VDD net1 di_D0 VSS 1u
G2 VDD net1 di_D1 VSS 2u
G3 VDD net1 di_D2 VSS 4u
G4 VDD net1 di_D3 VSS 8u
G5 VDD net1 di_D4 VSS 16u
G6 VDD net1 di_D5 VSS 32u
G7 VDD net1 di_D6 VSS 64u
G8 VDD net1 di_D7 VSS 128u
A1 net1 vdac_out VSS del_subckt
.model del_subckt delay(delay=tsettle buffer_size=8192)
.ends


* expanding   symbol:  comparator/continuous_time/ideal/CT_comparator_ideal.sym # of pins=5
** sym_path: SG13G2_ATBS-ADC-main/xschem/comparator/continuous_time/ideal/CT_comparator_ideal.sym
** sch_path: SG13G2_ATBS-ADC-main/xschem/comparator/continuous_time/ideal/CT_comparator_ideal.sch
.subckt CT_comparator_ideal vinp vinn VDD vout VSS  A=10k Rin=10Meg Rout=100 Vcm=0.75 Voffs=1m
+ tpd=1n
*.ipin vinn
*.opin vout
*.ipin vinp
*.iopin VSS
*.iopin VDD
R1 vinp vinn {Rin} m=1
B1 net1 VSS v=v(VDD)/2*tanh({A}/(v(VDD)/2)*(v(vinp)-v(vinn)-{Voffs}))+{Vcm}
R3 net2 vout {Rout} m=1
A1 net1 net2 VSS del_subckt
.model del_subckt delay(delay=tpd buffer_size=8192)
.ends

.GLOBAL GND
.end
